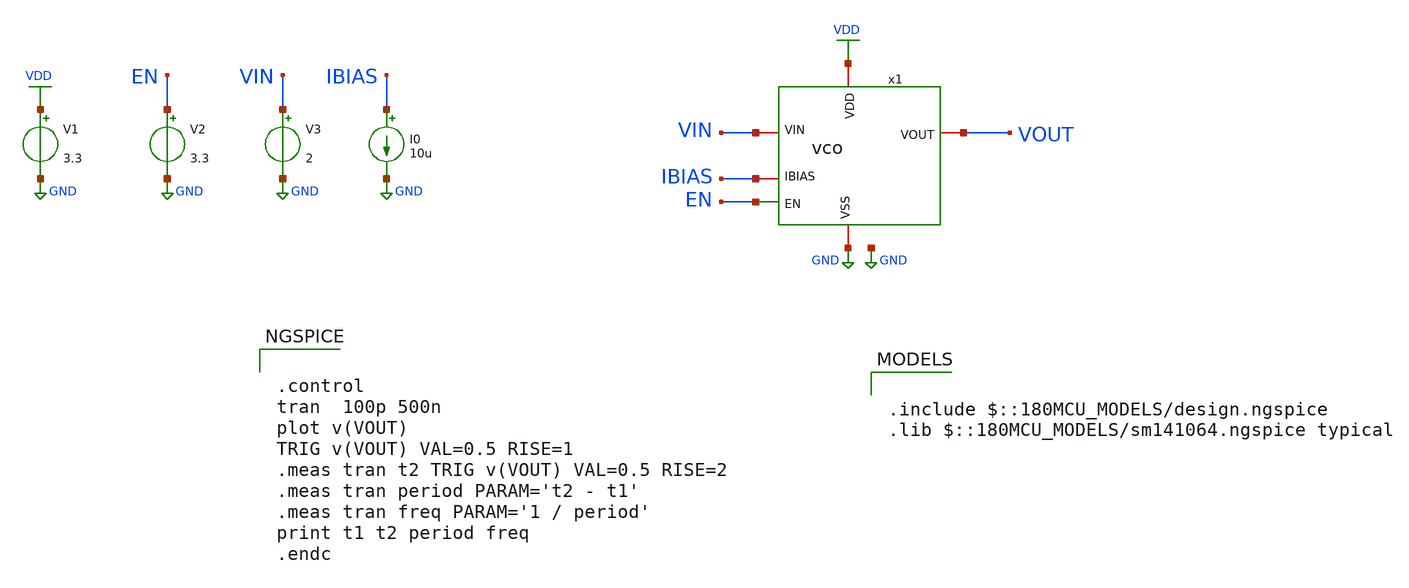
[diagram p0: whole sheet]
** sch_path: designs/libs/tb_vco/tb_vco/tb_vco.sch
**.subckt tb_vco
V1 VDD GND 3.3
V2 EN GND 3.3
V3 VIN GND 2
I0 IBIAS GND 10u
x1 VDD IBIAS VOUT EN GND VIN vco
**** begin user architecture code

.include $::180MCU_MODELS/design.ngspice
.lib $::180MCU_MODELS/sm141064.ngspice typical



.control
tran  100p 500n
plot v(VOUT)
TRIG v(VOUT) VAL=0.5 RISE=1
.meas tran t2 TRIG v(VOUT) VAL=0.5 RISE=2
.meas tran period PARAM='t2 - t1'
.meas tran freq PARAM='1 / period'
print t1 t2 period freq
.endc


**** end user architecture code
**.ends
.GLOBAL GND
.GLOBAL VDD
.end
